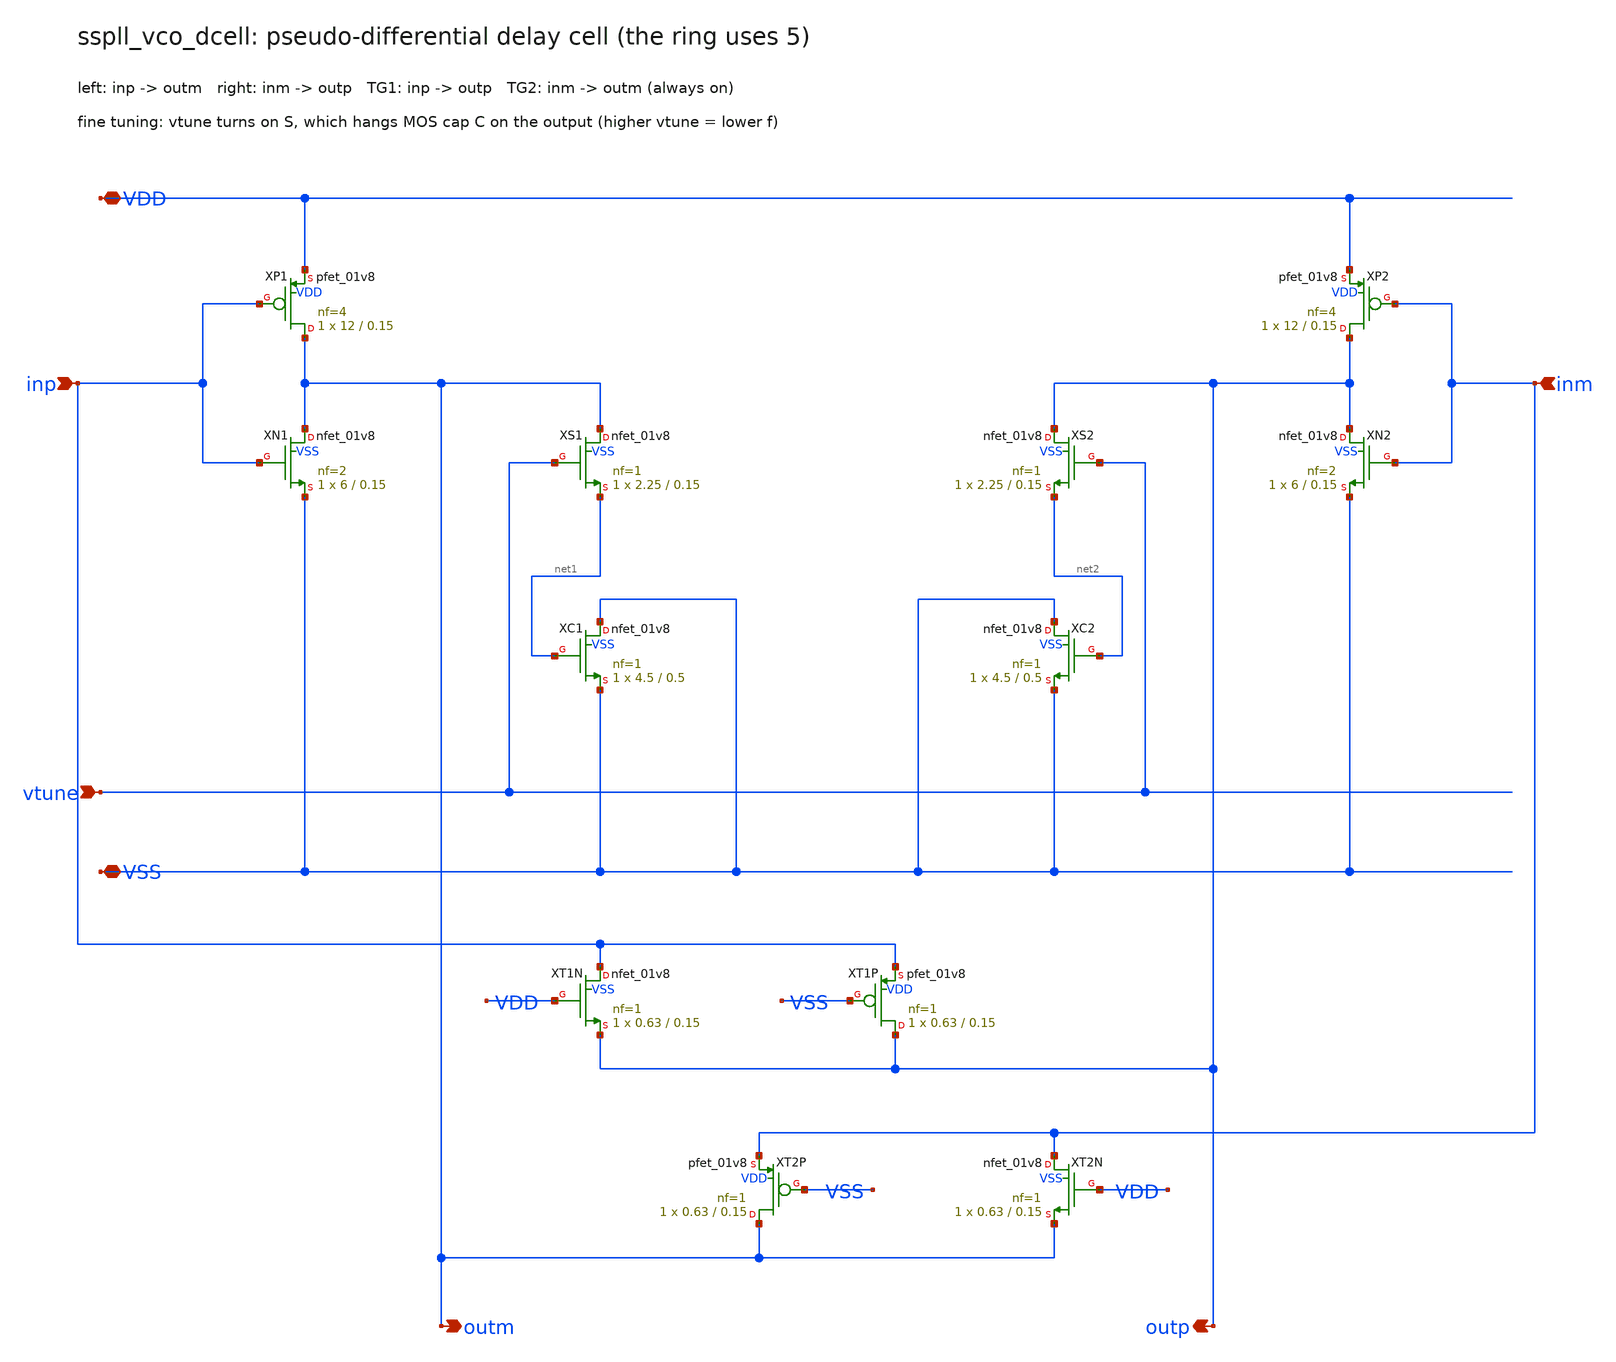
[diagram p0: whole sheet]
** sch_path: xschem/vco/sspll_vco_dcell.sch
**.subckt sspll_vco_dcell VDD VSS vtune inp inm outm outp
*.iopin VDD
*.iopin VSS
*.ipin vtune
*.ipin inp
*.ipin inm
*.opin outm
*.opin outp
XXP1 outm inp VDD VDD sky130_fd_pr__pfet_01v8 L=0.15 W=12 nf=4 ad='int((nf+1)/2) * W/nf * 0.29' as='int((nf+2)/2) * W/nf * 0.29'
+ pd='2*int((nf+1)/2) * (W/nf + 0.29)' ps='2*int((nf+2)/2) * (W/nf + 0.29)' nrd='0.29 / W' nrs='0.29 / W'
+ sa=0 sb=0 sd=0 mult=1 m=1
XXN1 outm inp VSS VSS sky130_fd_pr__nfet_01v8 L=0.15 W=6 nf=2 ad='int((nf+1)/2) * W/nf * 0.29' as='int((nf+2)/2) * W/nf * 0.29'
+ pd='2*int((nf+1)/2) * (W/nf + 0.29)' ps='2*int((nf+2)/2) * (W/nf + 0.29)' nrd='0.29 / W' nrs='0.29 / W'
+ sa=0 sb=0 sd=0 mult=1 m=1
XXS1 outm vtune net1 VSS sky130_fd_pr__nfet_01v8 L=0.15 W=2.25 nf=1 ad='int((nf+1)/2) * W/nf * 0.29'
+ as='int((nf+2)/2) * W/nf * 0.29' pd='2*int((nf+1)/2) * (W/nf + 0.29)' ps='2*int((nf+2)/2) * (W/nf + 0.29)'
+ nrd='0.29 / W' nrs='0.29 / W' sa=0 sb=0 sd=0 mult=1 m=1
XXC1 VSS net1 VSS VSS sky130_fd_pr__nfet_01v8 L=0.5 W=4.5 nf=1 ad='int((nf+1)/2) * W/nf * 0.29' as='int((nf+2)/2) * W/nf * 0.29'
+ pd='2*int((nf+1)/2) * (W/nf + 0.29)' ps='2*int((nf+2)/2) * (W/nf + 0.29)' nrd='0.29 / W' nrs='0.29 / W'
+ sa=0 sb=0 sd=0 mult=1 m=1
XXP2 outp inm VDD VDD sky130_fd_pr__pfet_01v8 L=0.15 W=12 nf=4 ad='int((nf+1)/2) * W/nf * 0.29' as='int((nf+2)/2) * W/nf * 0.29'
+ pd='2*int((nf+1)/2) * (W/nf + 0.29)' ps='2*int((nf+2)/2) * (W/nf + 0.29)' nrd='0.29 / W' nrs='0.29 / W'
+ sa=0 sb=0 sd=0 mult=1 m=1
XXN2 outp inm VSS VSS sky130_fd_pr__nfet_01v8 L=0.15 W=6 nf=2 ad='int((nf+1)/2) * W/nf * 0.29' as='int((nf+2)/2) * W/nf * 0.29'
+ pd='2*int((nf+1)/2) * (W/nf + 0.29)' ps='2*int((nf+2)/2) * (W/nf + 0.29)' nrd='0.29 / W' nrs='0.29 / W'
+ sa=0 sb=0 sd=0 mult=1 m=1
XXS2 outp vtune net2 VSS sky130_fd_pr__nfet_01v8 L=0.15 W=2.25 nf=1 ad='int((nf+1)/2) * W/nf * 0.29'
+ as='int((nf+2)/2) * W/nf * 0.29' pd='2*int((nf+1)/2) * (W/nf + 0.29)' ps='2*int((nf+2)/2) * (W/nf + 0.29)'
+ nrd='0.29 / W' nrs='0.29 / W' sa=0 sb=0 sd=0 mult=1 m=1
XXC2 VSS net2 VSS VSS sky130_fd_pr__nfet_01v8 L=0.5 W=4.5 nf=1 ad='int((nf+1)/2) * W/nf * 0.29' as='int((nf+2)/2) * W/nf * 0.29'
+ pd='2*int((nf+1)/2) * (W/nf + 0.29)' ps='2*int((nf+2)/2) * (W/nf + 0.29)' nrd='0.29 / W' nrs='0.29 / W'
+ sa=0 sb=0 sd=0 mult=1 m=1
XXT1N inp VDD outp VSS sky130_fd_pr__nfet_01v8 L=0.15 W=0.63 nf=1 ad='int((nf+1)/2) * W/nf * 0.29' as='int((nf+2)/2) * W/nf * 0.29'
+ pd='2*int((nf+1)/2) * (W/nf + 0.29)' ps='2*int((nf+2)/2) * (W/nf + 0.29)' nrd='0.29 / W' nrs='0.29 / W'
+ sa=0 sb=0 sd=0 mult=1 m=1
XXT1P outp VSS inp VDD sky130_fd_pr__pfet_01v8 L=0.15 W=0.63 nf=1 ad='int((nf+1)/2) * W/nf * 0.29' as='int((nf+2)/2) * W/nf * 0.29'
+ pd='2*int((nf+1)/2) * (W/nf + 0.29)' ps='2*int((nf+2)/2) * (W/nf + 0.29)' nrd='0.29 / W' nrs='0.29 / W'
+ sa=0 sb=0 sd=0 mult=1 m=1
XXT2N inm VDD outm VSS sky130_fd_pr__nfet_01v8 L=0.15 W=0.63 nf=1 ad='int((nf+1)/2) * W/nf * 0.29' as='int((nf+2)/2) * W/nf * 0.29'
+ pd='2*int((nf+1)/2) * (W/nf + 0.29)' ps='2*int((nf+2)/2) * (W/nf + 0.29)' nrd='0.29 / W' nrs='0.29 / W'
+ sa=0 sb=0 sd=0 mult=1 m=1
XXT2P outm VSS inm VDD sky130_fd_pr__pfet_01v8 L=0.15 W=0.63 nf=1 ad='int((nf+1)/2) * W/nf * 0.29' as='int((nf+2)/2) * W/nf * 0.29'
+ pd='2*int((nf+1)/2) * (W/nf + 0.29)' ps='2*int((nf+2)/2) * (W/nf + 0.29)' nrd='0.29 / W' nrs='0.29 / W'
+ sa=0 sb=0 sd=0 mult=1 m=1
**.ends
.end
